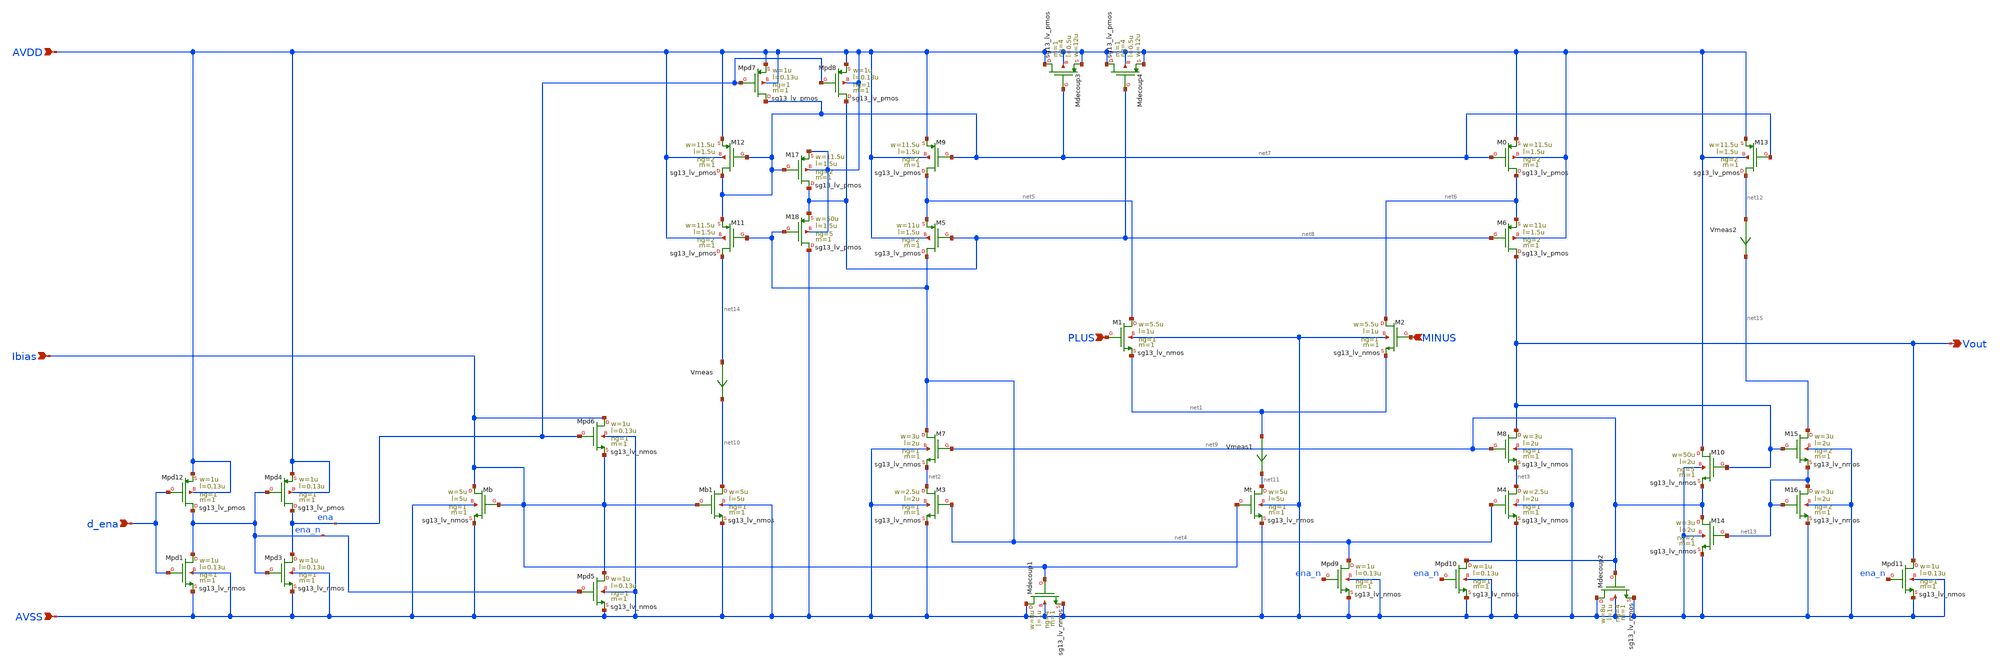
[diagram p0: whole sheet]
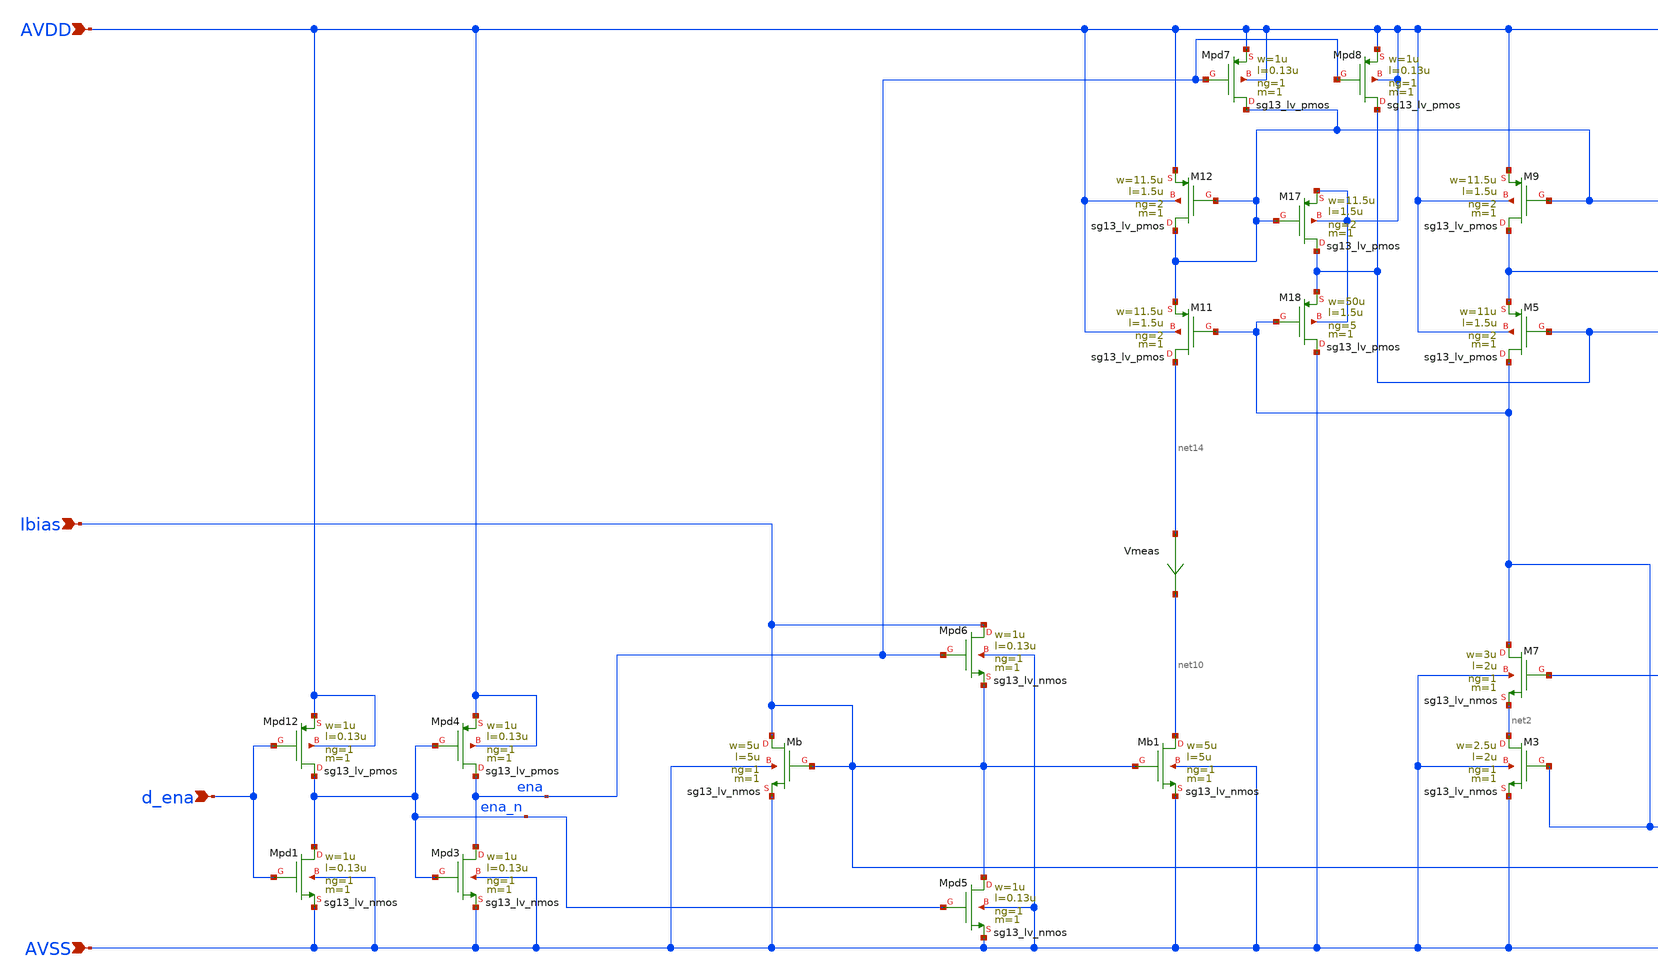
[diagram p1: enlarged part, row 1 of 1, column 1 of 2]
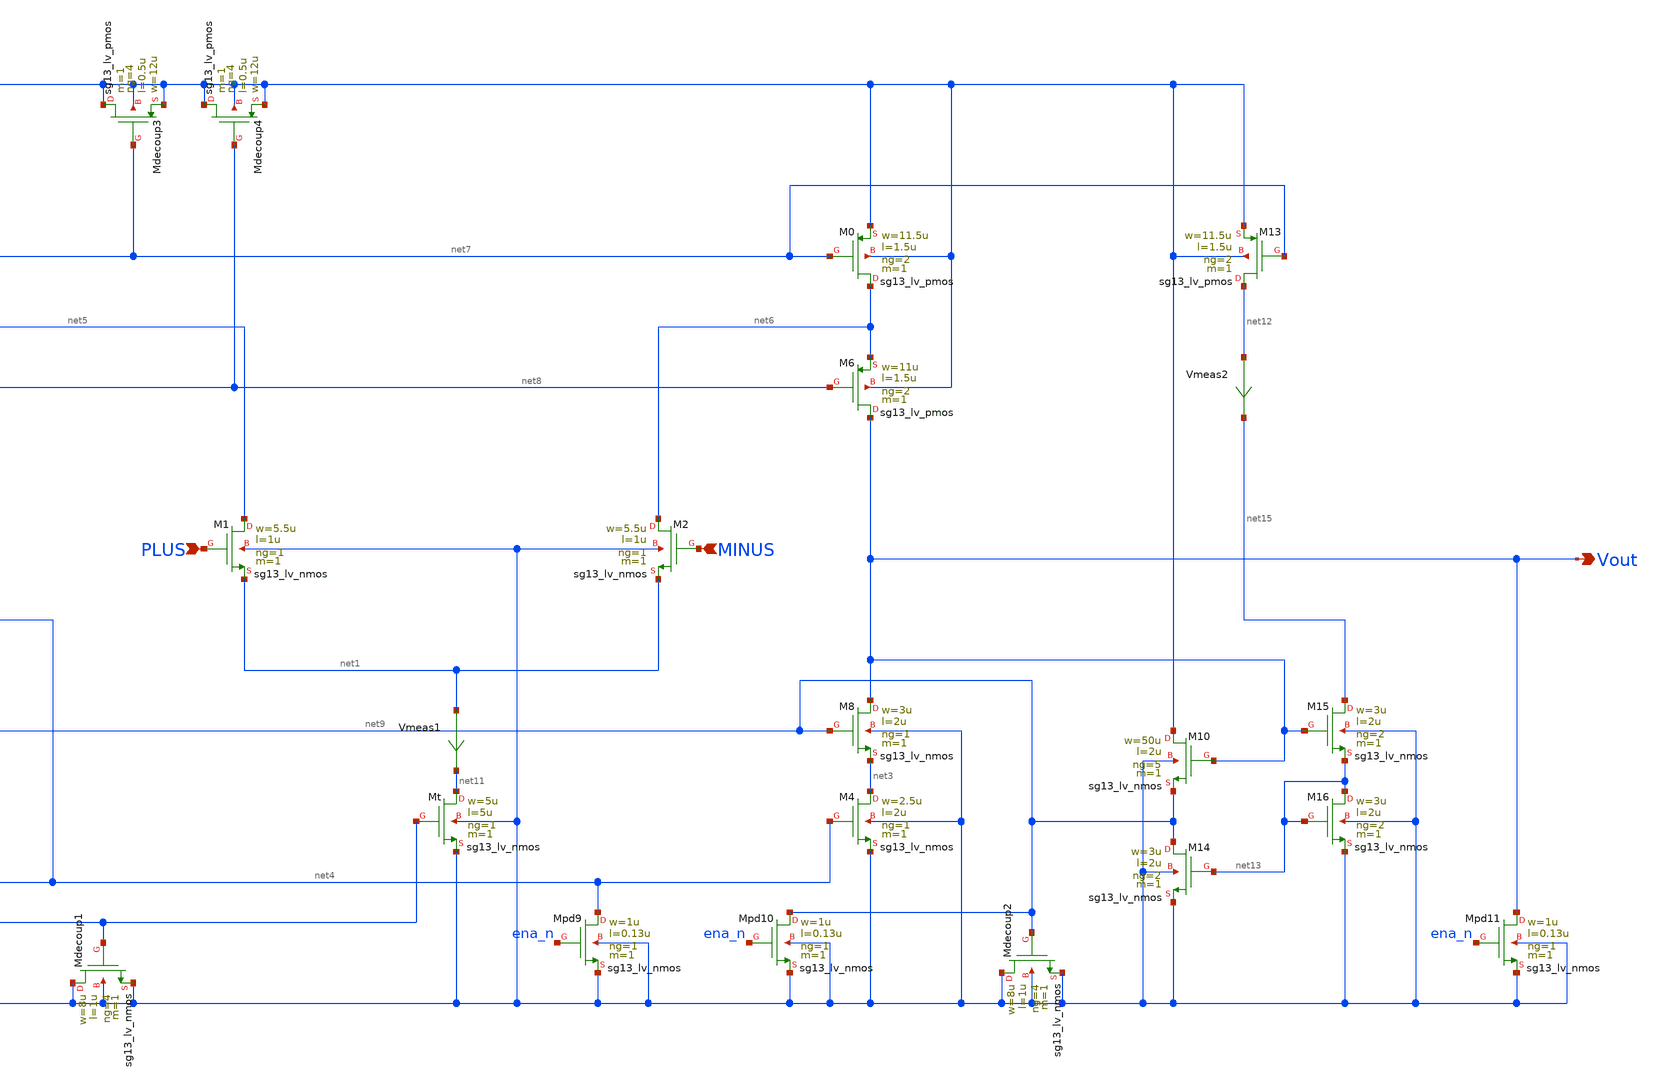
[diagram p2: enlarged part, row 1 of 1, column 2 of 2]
** sch_path: Designs/otas/1_schematics/foldedcascode_nmos.sch
* (c) 2025 Thesis_HP, Apache-2.0 license
**.subckt foldedcascode_nmos PLUS MINUS Vout AVDD AVSS Ibias d_ena
*.ipin PLUS
*.ipin MINUS
*.opin Vout
*.ipin AVDD
*.ipin AVSS
*.ipin Ibias
*.ipin d_ena
XM1 net5 PLUS net1 AVSS sg13_lv_nmos w=5.5u l=1u ng=1 m=1 mm_ok=1
XMt net11 Ibias AVSS AVSS sg13_lv_nmos w=5u l=5u ng=1 m=1 mm_ok=1
XM4 net3 net4 AVSS AVSS sg13_lv_nmos w=2.5u l=2u ng=1 m=1 mm_ok=1
XM3 net2 net4 AVSS AVSS sg13_lv_nmos w=2.5u l=2u ng=1 m=1 mm_ok=1
XM2 net6 MINUS net1 AVSS sg13_lv_nmos w=5.5u l=1u ng=1 m=1 mm_ok=1
XM7 net4 net9 net2 AVSS sg13_lv_nmos w=3u l=2u ng=1 m=1 mm_ok=1
XM8 Vout net9 net3 AVSS sg13_lv_nmos w=3u l=2u ng=1 m=1 mm_ok=1
XM5 net4 net8 net5 AVDD sg13_lv_pmos w=11u l=1.5u ng=2 m=1 mm_ok=1
XM9 net5 net7 AVDD AVDD sg13_lv_pmos w=11.5u l=1.5u ng=2 m=1 mm_ok=1
XM6 Vout net8 net6 AVDD sg13_lv_pmos w=11u l=1.5u ng=2 m=1 mm_ok=1
XM0 net6 net7 AVDD AVDD sg13_lv_pmos w=11.5u l=1.5u ng=2 m=1 mm_ok=1
XMb Ibias Ibias AVSS AVSS sg13_lv_nmos w=5u l=5u ng=1 m=1 mm_ok=1
XM11 net14 net4 net7 AVDD sg13_lv_pmos w=11.5u l=1.5u ng=2 m=1 mm_ok=1
XM12 net7 net7 AVDD AVDD sg13_lv_pmos w=11.5u l=1.5u ng=2 m=1 mm_ok=1
XM13 net12 net7 AVDD AVDD sg13_lv_pmos w=11.5u l=1.5u ng=2 m=1 mm_ok=1
XMb1 net10 Ibias AVSS AVSS sg13_lv_nmos w=5u l=5u ng=1 m=1 mm_ok=1
Vmeas net14 net10 0
.save i(vmeas)
Vmeas1 net1 net11 0
.save i(vmeas1)
Vmeas2 net12 net15 0
.save i(vmeas2)
XMdecoup1 AVSS Ibias AVSS AVSS sg13_lv_nmos w=8u l=1u ng=4 m=1 mm_ok=1
XMdecoup2 AVSS net9 AVSS AVSS sg13_lv_nmos w=8u l=1u ng=4 m=1 mm_ok=1
XMdecoup3 AVDD net7 AVDD AVDD sg13_lv_pmos w=12u l=0.5u ng=4 m=1 mm_ok=1
XMdecoup4 AVDD net8 AVDD AVDD sg13_lv_pmos w=12u l=0.5u ng=4 m=1 mm_ok=1
XMpd3 ena ena_n AVSS AVSS sg13_lv_nmos w=1u l=0.13u ng=1 m=1 mm_ok=1
XMpd4 ena ena_n AVDD AVDD sg13_lv_pmos w=1u l=0.13u ng=1 m=1 mm_ok=1
XMpd1 ena_n d_ena AVSS AVSS sg13_lv_nmos w=1u l=0.13u ng=1 m=1 mm_ok=1
XMpd5 Ibias ena_n AVSS AVSS sg13_lv_nmos w=1u l=0.13u ng=1 m=1 mm_ok=1
XMpd6 Ibias ena Ibias AVSS sg13_lv_nmos w=1u l=0.13u ng=1 m=1 mm_ok=1
XMpd7 net7 ena AVDD AVDD sg13_lv_pmos w=1u l=0.13u ng=1 m=1 mm_ok=1
XMpd8 net8 ena AVDD AVDD sg13_lv_pmos w=1u l=0.13u ng=1 m=1 mm_ok=1
XMpd9 net4 ena_n AVSS AVSS sg13_lv_nmos w=1u l=0.13u ng=1 m=1 mm_ok=1
XMpd10 net9 ena_n AVSS AVSS sg13_lv_nmos w=1u l=0.13u ng=1 m=1 mm_ok=1
XMpd11 Vout ena_n AVSS AVSS sg13_lv_nmos w=1u l=0.13u ng=1 m=1 mm_ok=1
XM15 net15 Vout net13 AVSS sg13_lv_nmos w=3u l=2u ng=2 m=1 mm_ok=1
XM16 net13 net13 AVSS AVSS sg13_lv_nmos w=3u l=2u ng=2 m=1 mm_ok=1
XM10 AVDD Vout net9 AVSS sg13_lv_nmos w=50u l=2u ng=5 m=1 mm_ok=1
XM14 net9 net13 AVSS AVSS sg13_lv_nmos w=3u l=2u ng=2 m=1 mm_ok=1
XM17 net8 net7 AVDD AVDD sg13_lv_pmos w=11.5u l=1.5u ng=2 m=1 mm_ok=1
XM18 AVSS net4 net8 AVDD sg13_lv_pmos w=50u l=1.5u ng=5 m=1 mm_ok=1
XMpd12 ena_n d_ena AVDD AVDD sg13_lv_pmos w=1u l=0.13u ng=1 m=1 mm_ok=1
**.ends
.end
